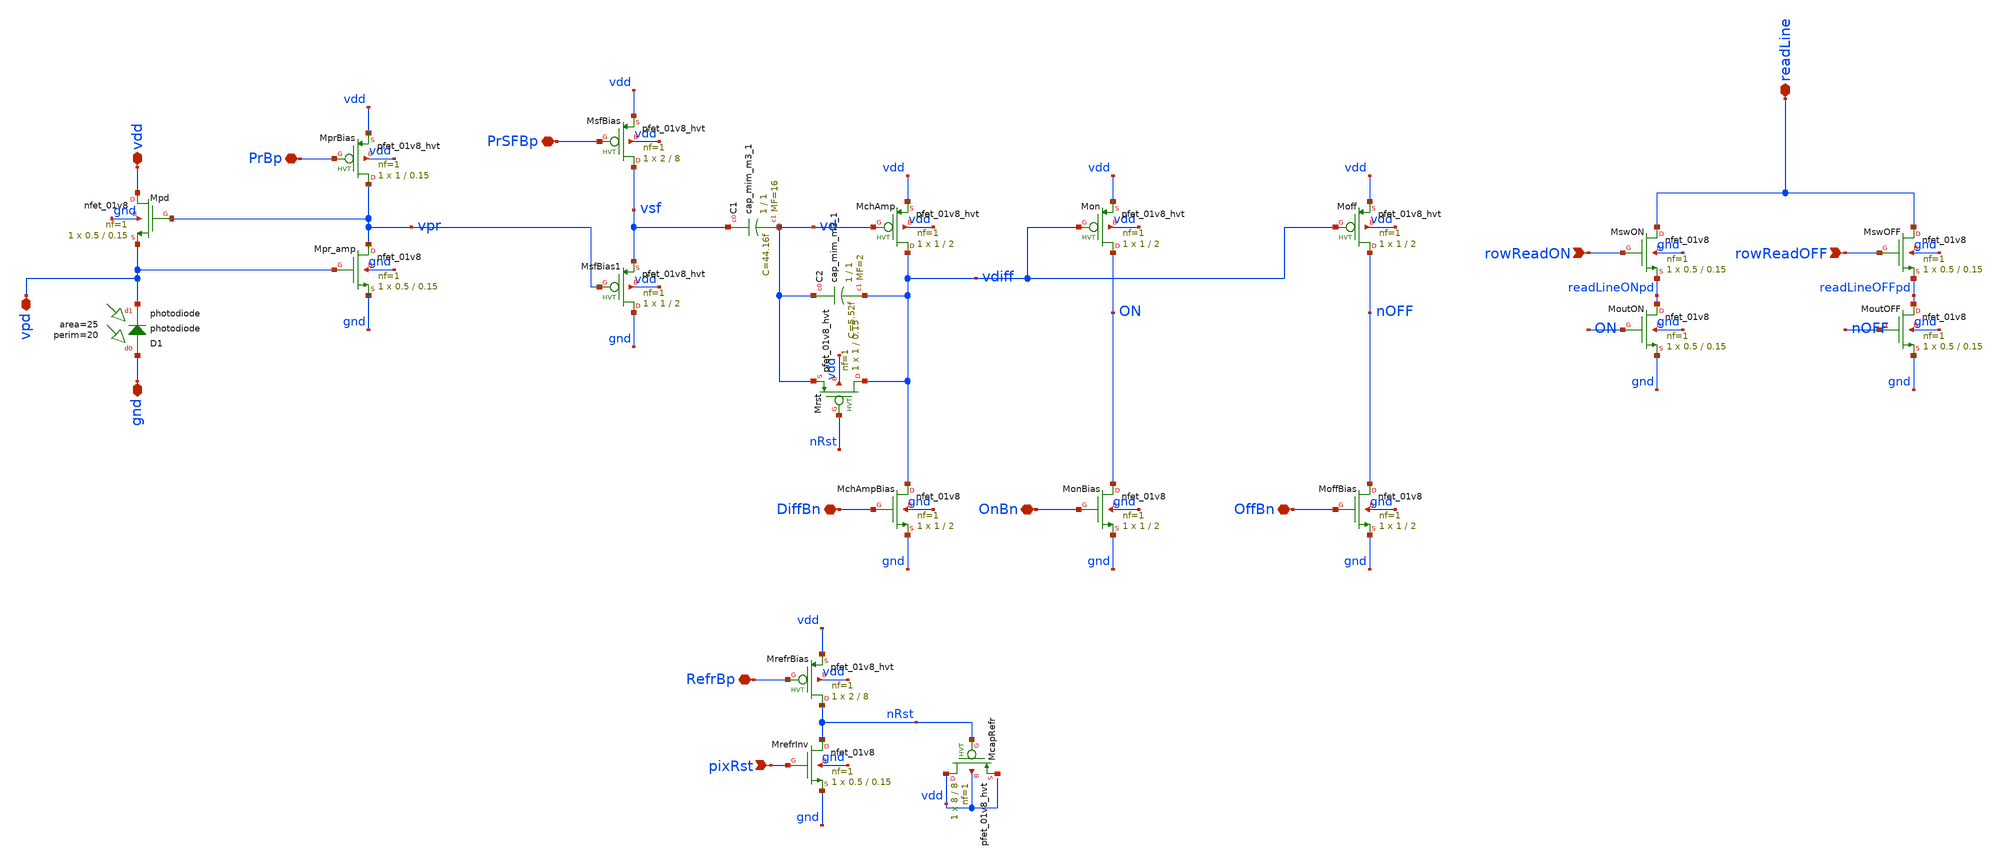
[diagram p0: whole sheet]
** sch_path: analog/xschem/openDVS_pixel.sch
**.subckt openDVS_pixel rowReadON PrBp vdd vpd PrSFBp gnd DiffBn OnBn OffBn rowReadOFF readLine
*+ pixRst RefrBp
*.ipin rowReadON
*.iopin PrBp
*.iopin vdd
*.iopin vpd
*.iopin PrSFBp
*.iopin gnd
*.iopin DiffBn
*.iopin OnBn
*.iopin OffBn
*.ipin rowReadOFF
*.iopin readLine
*.ipin pixRst
*.iopin RefrBp
XC1 vsf vd sky130_fd_pr__cap_mim_m3_1 W=1 L=1 MF=16 m=16
XMpd vdd vpr vpd gnd sky130_fd_pr__nfet_01v8 L=0.15 W=0.5 nf=1 ad='int((1 + 1)/2) * 0.5 / 1 * 0.29' as='int((1 + 2)/2) * 0.5 / 1 * 0.29'
+ pd='2*int((1 + 1)/2) * (0.5 / 1 + 0.29)' ps='2*int((1 + 2)/2) * (0.5 / 1 + 0.29)' nrd='0.29 / 0.5 ' nrs='0.29 / 0.5 '
+ sa=0 sb=0 sd=0 mult=1 m=1
XMpr_amp vpr vpd gnd gnd sky130_fd_pr__nfet_01v8 L=0.15 W=0.5 nf=1 ad='int((1 + 1)/2) * 0.5 / 1 * 0.29'
+ as='int((1 + 2)/2) * 0.5 / 1 * 0.29' pd='2*int((1 + 1)/2) * (0.5 / 1 + 0.29)' ps='2*int((1 + 2)/2) * (0.5 / 1 + 0.29)'
+ nrd='0.29 / 0.5 ' nrs='0.29 / 0.5 ' sa=0 sb=0 sd=0 mult=1 m=1
XD1 gnd vpd sky130_fd_pr__photodiode area=25 perim=20
XC2 vd vdiff sky130_fd_pr__cap_mim_m3_1 W=1 L=1 MF=2 m=2
XMchAmpBias vdiff DiffBn gnd gnd sky130_fd_pr__nfet_01v8 L=2 W=1 nf=1 ad='int((1 + 1)/2) * 1 / 1 * 0.29'
+ as='int((1 + 2)/2) * 1 / 1 * 0.29' pd='2*int((1 + 1)/2) * (1 / 1 + 0.29)' ps='2*int((1 + 2)/2) * (1 / 1 + 0.29)'
+ nrd='0.29 / 1 ' nrs='0.29 / 1 ' sa=0 sb=0 sd=0 mult=1 m=1
XMonBias ON OnBn gnd gnd sky130_fd_pr__nfet_01v8 L=2 W=1 nf=1 ad='int((1 + 1)/2) * 1 / 1 * 0.29' as='int((1 + 2)/2) * 1 / 1 * 0.29'
+ pd='2*int((1 + 1)/2) * (1 / 1 + 0.29)' ps='2*int((1 + 2)/2) * (1 / 1 + 0.29)' nrd='0.29 / 1 ' nrs='0.29 / 1 '
+ sa=0 sb=0 sd=0 mult=1 m=1
XMoffBias nOFF OffBn gnd gnd sky130_fd_pr__nfet_01v8 L=2 W=1 nf=1 ad='int((1 + 1)/2) * 1 / 1 * 0.29'
+ as='int((1 + 2)/2) * 1 / 1 * 0.29' pd='2*int((1 + 1)/2) * (1 / 1 + 0.29)' ps='2*int((1 + 2)/2) * (1 / 1 + 0.29)'
+ nrd='0.29 / 1 ' nrs='0.29 / 1 ' sa=0 sb=0 sd=0 mult=1 m=1
XMswON readLine rowReadON readLineONpd gnd sky130_fd_pr__nfet_01v8 L=0.15 W=0.5 nf=1 ad='int((1 + 1)/2) * 0.5 / 1 * 0.29'
+ as='int((1 + 2)/2) * 0.5 / 1 * 0.29' pd='2*int((1 + 1)/2) * (0.5 / 1 + 0.29)' ps='2*int((1 + 2)/2) * (0.5 / 1 + 0.29)'
+ nrd='0.29 / 0.5 ' nrs='0.29 / 0.5 ' sa=0 sb=0 sd=0 mult=1 m=1
XMoutON readLineONpd ON gnd gnd sky130_fd_pr__nfet_01v8 L=0.15 W=0.5 nf=1 ad='int((1 + 1)/2) * 0.5 / 1 * 0.29'
+ as='int((1 + 2)/2) * 0.5 / 1 * 0.29' pd='2*int((1 + 1)/2) * (0.5 / 1 + 0.29)' ps='2*int((1 + 2)/2) * (0.5 / 1 + 0.29)'
+ nrd='0.29 / 0.5 ' nrs='0.29 / 0.5 ' sa=0 sb=0 sd=0 mult=1 m=1
XMswOFF readLine rowReadOFF readLineOFFpd gnd sky130_fd_pr__nfet_01v8 L=0.15 W=0.5 nf=1 ad='int((1 + 1)/2) * 0.5 / 1 * 0.29'
+ as='int((1 + 2)/2) * 0.5 / 1 * 0.29' pd='2*int((1 + 1)/2) * (0.5 / 1 + 0.29)' ps='2*int((1 + 2)/2) * (0.5 / 1 + 0.29)'
+ nrd='0.29 / 0.5 ' nrs='0.29 / 0.5 ' sa=0 sb=0 sd=0 mult=1 m=1
XMoutOFF readLineOFFpd nOFF gnd gnd sky130_fd_pr__nfet_01v8 L=0.15 W=0.5 nf=1 ad='int((1 + 1)/2) * 0.5 / 1 * 0.29'
+ as='int((1 + 2)/2) * 0.5 / 1 * 0.29' pd='2*int((1 + 1)/2) * (0.5 / 1 + 0.29)' ps='2*int((1 + 2)/2) * (0.5 / 1 + 0.29)'
+ nrd='0.29 / 0.5 ' nrs='0.29 / 0.5 ' sa=0 sb=0 sd=0 mult=1 m=1
XMrst vdiff nRst vd vdd sky130_fd_pr__pfet_01v8_hvt L=0.15 W=1 nf=1 ad='int((1 + 1)/2) * 1 / 1 * 0.29'
+ as='int((1 + 2)/2) * 1 / 1 * 0.29' pd='2*int((1 + 1)/2) * (1 / 1 + 0.29)' ps='2*int((1 + 2)/2) * (1 / 1 + 0.29)'
+ nrd='0.29 / 1 ' nrs='0.29 / 1 ' sa=0 sb=0 sd=0 mult=1 m=1
XMprBias vpr PrBp vdd vdd sky130_fd_pr__pfet_01v8_hvt L=0.15 W=1 nf=1 ad='int((1 + 1)/2) * 1 / 1 * 0.29'
+ as='int((1 + 2)/2) * 1 / 1 * 0.29' pd='2*int((1 + 1)/2) * (1 / 1 + 0.29)' ps='2*int((1 + 2)/2) * (1 / 1 + 0.29)'
+ nrd='0.29 / 1 ' nrs='0.29 / 1 ' sa=0 sb=0 sd=0 mult=1 m=1
XMsfBias vsf PrSFBp vdd vdd sky130_fd_pr__pfet_01v8_hvt L=8 W=2 nf=1 ad='int((1 + 1)/2) * 2 / 1 * 0.29'
+ as='int((1 + 2)/2) * 2 / 1 * 0.29' pd='2*int((1 + 1)/2) * (2 / 1 + 0.29)' ps='2*int((1 + 2)/2) * (2 / 1 + 0.29)'
+ nrd='0.29 / 2 ' nrs='0.29 / 2 ' sa=0 sb=0 sd=0 mult=1 m=1
XMchAmp vdiff vd vdd vdd sky130_fd_pr__pfet_01v8_hvt L=2 W=1 nf=1 ad='int((1 + 1)/2) * 1 / 1 * 0.29'
+ as='int((1 + 2)/2) * 1 / 1 * 0.29' pd='2*int((1 + 1)/2) * (1 / 1 + 0.29)' ps='2*int((1 + 2)/2) * (1 / 1 + 0.29)'
+ nrd='0.29 / 1 ' nrs='0.29 / 1 ' sa=0 sb=0 sd=0 mult=1 m=1
XMon ON vdiff vdd vdd sky130_fd_pr__pfet_01v8_hvt L=2 W=1 nf=1 ad='int((1 + 1)/2) * 1 / 1 * 0.29' as='int((1 + 2)/2) * 1 / 1 * 0.29'
+ pd='2*int((1 + 1)/2) * (1 / 1 + 0.29)' ps='2*int((1 + 2)/2) * (1 / 1 + 0.29)' nrd='0.29 / 1 ' nrs='0.29 / 1 '
+ sa=0 sb=0 sd=0 mult=1 m=1
XMoff nOFF vdiff vdd vdd sky130_fd_pr__pfet_01v8_hvt L=2 W=1 nf=1 ad='int((1 + 1)/2) * 1 / 1 * 0.29'
+ as='int((1 + 2)/2) * 1 / 1 * 0.29' pd='2*int((1 + 1)/2) * (1 / 1 + 0.29)' ps='2*int((1 + 2)/2) * (1 / 1 + 0.29)'
+ nrd='0.29 / 1 ' nrs='0.29 / 1 ' sa=0 sb=0 sd=0 mult=1 m=1
XMrefrInv nRst pixRst gnd gnd sky130_fd_pr__nfet_01v8 L=0.15 W=0.5 nf=1 ad='int((1 + 1)/2) * 0.5 / 1 * 0.29'
+ as='int((1 + 2)/2) * 0.5 / 1 * 0.29' pd='2*int((1 + 1)/2) * (0.5 / 1 + 0.29)' ps='2*int((1 + 2)/2) * (0.5 / 1 + 0.29)'
+ nrd='0.29 / 0.5 ' nrs='0.29 / 0.5 ' sa=0 sb=0 sd=0 mult=1 m=1
XMrefrBias nRst RefrBp vdd vdd sky130_fd_pr__pfet_01v8_hvt L=8 W=2 nf=1 ad='int((1 + 1)/2) * 2 / 1 * 0.29'
+ as='int((1 + 2)/2) * 2 / 1 * 0.29' pd='2*int((1 + 1)/2) * (2 / 1 + 0.29)' ps='2*int((1 + 2)/2) * (2 / 1 + 0.29)'
+ nrd='0.29 / 2 ' nrs='0.29 / 2 ' sa=0 sb=0 sd=0 mult=1 m=1
XMcapRefr vdd nRst net1 vdd sky130_fd_pr__pfet_01v8_hvt L=8 W=8 nf=1 ad='int((1 + 1)/2) * 8 / 1 * 0.29'
+ as='int((1 + 2)/2) * 8 / 1 * 0.29' pd='2*int((1 + 1)/2) * (8 / 1 + 0.29)' ps='2*int((1 + 2)/2) * (8 / 1 + 0.29)'
+ nrd='0.29 / 8 ' nrs='0.29 / 8 ' sa=0 sb=0 sd=0 mult=1 m=1
XMsfBias1 gnd vpr vsf vdd sky130_fd_pr__pfet_01v8_hvt L=2 W=1 nf=1 ad='int((1 + 1)/2) * 1 / 1 * 0.29'
+ as='int((1 + 2)/2) * 1 / 1 * 0.29' pd='2*int((1 + 1)/2) * (1 / 1 + 0.29)' ps='2*int((1 + 2)/2) * (1 / 1 + 0.29)'
+ nrd='0.29 / 1 ' nrs='0.29 / 1 ' sa=0 sb=0 sd=0 mult=1 m=1
**.ends
.end
